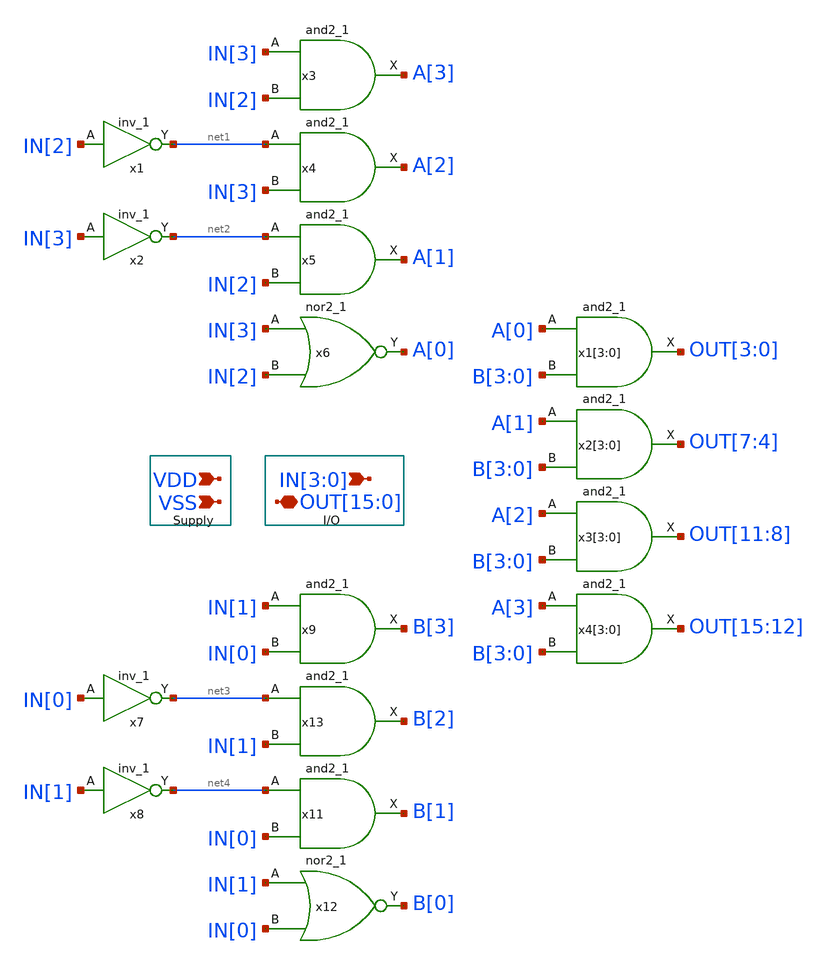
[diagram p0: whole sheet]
** sch_path: BL_SL_Writing_Interface/decoder_4_to_16_5V.sch
**.subckt decoder_4_to_16_5V VSS VDD IN[3],IN[2],IN[1],IN[0]
*+ OUT[15],OUT[14],OUT[13],OUT[12],OUT[11],OUT[10],OUT[9],OUT[8],OUT[7],OUT[6],OUT[5],OUT[4],OUT[3],OUT[2],OUT[1],OUT[0]
*.ipin VSS
*.ipin VDD
*.ipin IN[3],IN[2],IN[1],IN[0]
*.iopin
*+ OUT[15],OUT[14],OUT[13],OUT[12],OUT[11],OUT[10],OUT[9],OUT[8],OUT[7],OUT[6],OUT[5],OUT[4],OUT[3],OUT[2],OUT[1],OUT[0]
x1 IN[2] VSS VSS VDD VDD net1 sky130_fd_sc_hvl__inv_1
x2 IN[3] VSS VSS VDD VDD net2 sky130_fd_sc_hvl__inv_1
x3 IN[3] IN[2] VSS VSS VDD VDD A[3] sky130_fd_sc_hvl__and2_1
x4 net1 IN[3] VSS VSS VDD VDD A[2] sky130_fd_sc_hvl__and2_1
x5 net2 IN[2] VSS VSS VDD VDD A[1] sky130_fd_sc_hvl__and2_1
x7 IN[0] VSS VSS VDD VDD net3 sky130_fd_sc_hvl__inv_1
x8 IN[1] VSS VSS VDD VDD net4 sky130_fd_sc_hvl__inv_1
x9 IN[1] IN[0] VSS VSS VDD VDD B[3] sky130_fd_sc_hvl__and2_1
x6 IN[3] IN[2] VSS VSS VDD VDD A[0] sky130_fd_sc_hvl__nor2_1
x3[3] A[2] B[3] VSS VSS VDD VDD OUT[11] sky130_fd_sc_hvl__and2_1
x3[2] A[2] B[2] VSS VSS VDD VDD OUT[10] sky130_fd_sc_hvl__and2_1
x3[1] A[2] B[1] VSS VSS VDD VDD OUT[9] sky130_fd_sc_hvl__and2_1
x3[0] A[2] B[0] VSS VSS VDD VDD OUT[8] sky130_fd_sc_hvl__and2_1
x1[3] A[0] B[3] VSS VSS VDD VDD OUT[3] sky130_fd_sc_hvl__and2_1
x1[2] A[0] B[2] VSS VSS VDD VDD OUT[2] sky130_fd_sc_hvl__and2_1
x1[1] A[0] B[1] VSS VSS VDD VDD OUT[1] sky130_fd_sc_hvl__and2_1
x1[0] A[0] B[0] VSS VSS VDD VDD OUT[0] sky130_fd_sc_hvl__and2_1
x2[3] A[1] B[3] VSS VSS VDD VDD OUT[7] sky130_fd_sc_hvl__and2_1
x2[2] A[1] B[2] VSS VSS VDD VDD OUT[6] sky130_fd_sc_hvl__and2_1
x2[1] A[1] B[1] VSS VSS VDD VDD OUT[5] sky130_fd_sc_hvl__and2_1
x2[0] A[1] B[0] VSS VSS VDD VDD OUT[4] sky130_fd_sc_hvl__and2_1
x4[3] A[3] B[3] VSS VSS VDD VDD OUT[15] sky130_fd_sc_hvl__and2_1
x4[2] A[3] B[2] VSS VSS VDD VDD OUT[14] sky130_fd_sc_hvl__and2_1
x4[1] A[3] B[1] VSS VSS VDD VDD OUT[13] sky130_fd_sc_hvl__and2_1
x4[0] A[3] B[0] VSS VSS VDD VDD OUT[12] sky130_fd_sc_hvl__and2_1
x13 net3 IN[1] VSS VSS VDD VDD B[2] sky130_fd_sc_hvl__and2_1
x11 net4 IN[0] VSS VSS VDD VDD B[1] sky130_fd_sc_hvl__and2_1
x12 IN[1] IN[0] VSS VSS VDD VDD B[0] sky130_fd_sc_hvl__nor2_1
**.ends
.end
